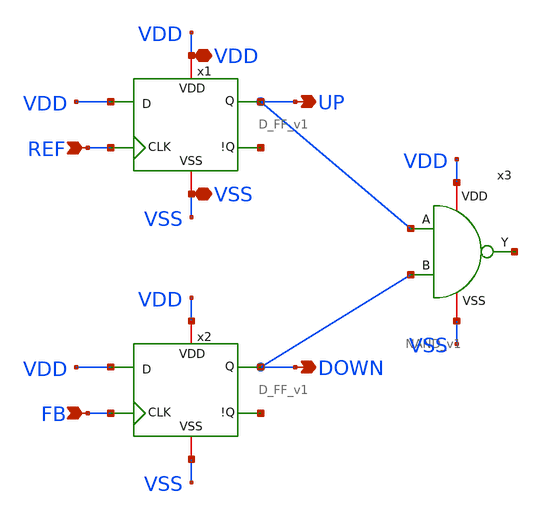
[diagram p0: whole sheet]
** sch_path: team_src/xschem/PFD_v1.sch
**.subckt PFD_v1 REF VSS VDD UP FB DOWN
*.ipin REF
*.iopin VSS
*.iopin VDD
*.opin UP
*.ipin FB
*.opin DOWN
x1 VDD VDD UP REF net1 VSS D_FF_v1
x2 VDD VDD DOWN FB net2 VSS D_FF_v1
x3 VDD net3 UP DOWN VSS NAND_v1
**.ends

* expanding   symbol:  D_FF_v1.sym # of pins=6
** sym_path: team_src/xschem/D_FF_v1.sym
** sch_path: team_src/xschem/D_FF_v1.sch
.subckt D_FF_v1 VDD D Q CLK !Q VSS
*.ipin CLK
*.ipin D
*.iopin VDD
*.opin Q
*.opin !Q
*.iopin VSS
x1 VDD Q net1 !Q VSS NAND_v1
x2 VDD !Q Q net2 VSS NAND_v1
x3 VDD net1 D net4 VSS NAND_v1
x4 VDD net2 net3 net4 VSS NAND_v1
x5 VDD D net3 VSS NOT_v1
x6 VDD net5 net4 VSS NOT_v1
x7 VDD CLK net6 VSS NOT_v1
x8 VDD net5 CLK net6 VSS NAND_v1
.ends


* expanding   symbol:  NAND_v1.sym # of pins=5
** sym_path: team_src/xschem/NAND_v1.sym
** sch_path: team_src/xschem/NAND_v1.sch
.subckt NAND_v1 VDD Y A B VSS
*.iopin VSS
*.iopin VDD
*.ipin A
*.opin Y
*.ipin B
XM1 net1 B VSS VSS nfet_03v3 L=0.28u W=1u nf=1 ad='int((nf+1)/2) * W/nf * 0.18u' as='int((nf+2)/2) * W/nf * 0.18u'
+ pd='2*int((nf+1)/2) * (W/nf + 0.18u)' ps='2*int((nf+2)/2) * (W/nf + 0.18u)' nrd='0.18u / W' nrs='0.18u / W'
+ sa=0 sb=0 sd=0 m=1
XM2 Y A net1 VSS nfet_03v3 L=0.28u W=1u nf=1 ad='int((nf+1)/2) * W/nf * 0.18u' as='int((nf+2)/2) * W/nf * 0.18u'
+ pd='2*int((nf+1)/2) * (W/nf + 0.18u)' ps='2*int((nf+2)/2) * (W/nf + 0.18u)' nrd='0.18u / W' nrs='0.18u / W'
+ sa=0 sb=0 sd=0 m=1
XM3 Y B VDD VDD pfet_03v3 L=0.28u W=1u nf=1 ad='int((nf+1)/2) * W/nf * 0.18u' as='int((nf+2)/2) * W/nf * 0.18u'
+ pd='2*int((nf+1)/2) * (W/nf + 0.18u)' ps='2*int((nf+2)/2) * (W/nf + 0.18u)' nrd='0.18u / W' nrs='0.18u / W'
+ sa=0 sb=0 sd=0 m=1
XM4 Y A VDD VDD pfet_03v3 L=0.28u W=1u nf=1 ad='int((nf+1)/2) * W/nf * 0.18u' as='int((nf+2)/2) * W/nf * 0.18u'
+ pd='2*int((nf+1)/2) * (W/nf + 0.18u)' ps='2*int((nf+2)/2) * (W/nf + 0.18u)' nrd='0.18u / W' nrs='0.18u / W'
+ sa=0 sb=0 sd=0 m=1
.ends


* expanding   symbol:  NOT_v1.sym # of pins=4
** sym_path: team_src/xschem/NOT_v1.sym
** sch_path: team_src/xschem/NOT_v1.sch
.subckt NOT_v1 VDD A Y VSS
*.iopin VSS
*.iopin VDD
*.ipin A
*.opin Y
XM2 Y A VSS VSS nfet_03v3 L=0.28u W=1u nf=1 ad='int((nf+1)/2) * W/nf * 0.18u' as='int((nf+2)/2) * W/nf * 0.18u'
+ pd='2*int((nf+1)/2) * (W/nf + 0.18u)' ps='2*int((nf+2)/2) * (W/nf + 0.18u)' nrd='0.18u / W' nrs='0.18u / W'
+ sa=0 sb=0 sd=0 m=1
XM4 Y A VDD VDD pfet_03v3 L=0.28u W=1u nf=1 ad='int((nf+1)/2) * W/nf * 0.18u' as='int((nf+2)/2) * W/nf * 0.18u'
+ pd='2*int((nf+1)/2) * (W/nf + 0.18u)' ps='2*int((nf+2)/2) * (W/nf + 0.18u)' nrd='0.18u / W' nrs='0.18u / W'
+ sa=0 sb=0 sd=0 m=1
.ends

.end
